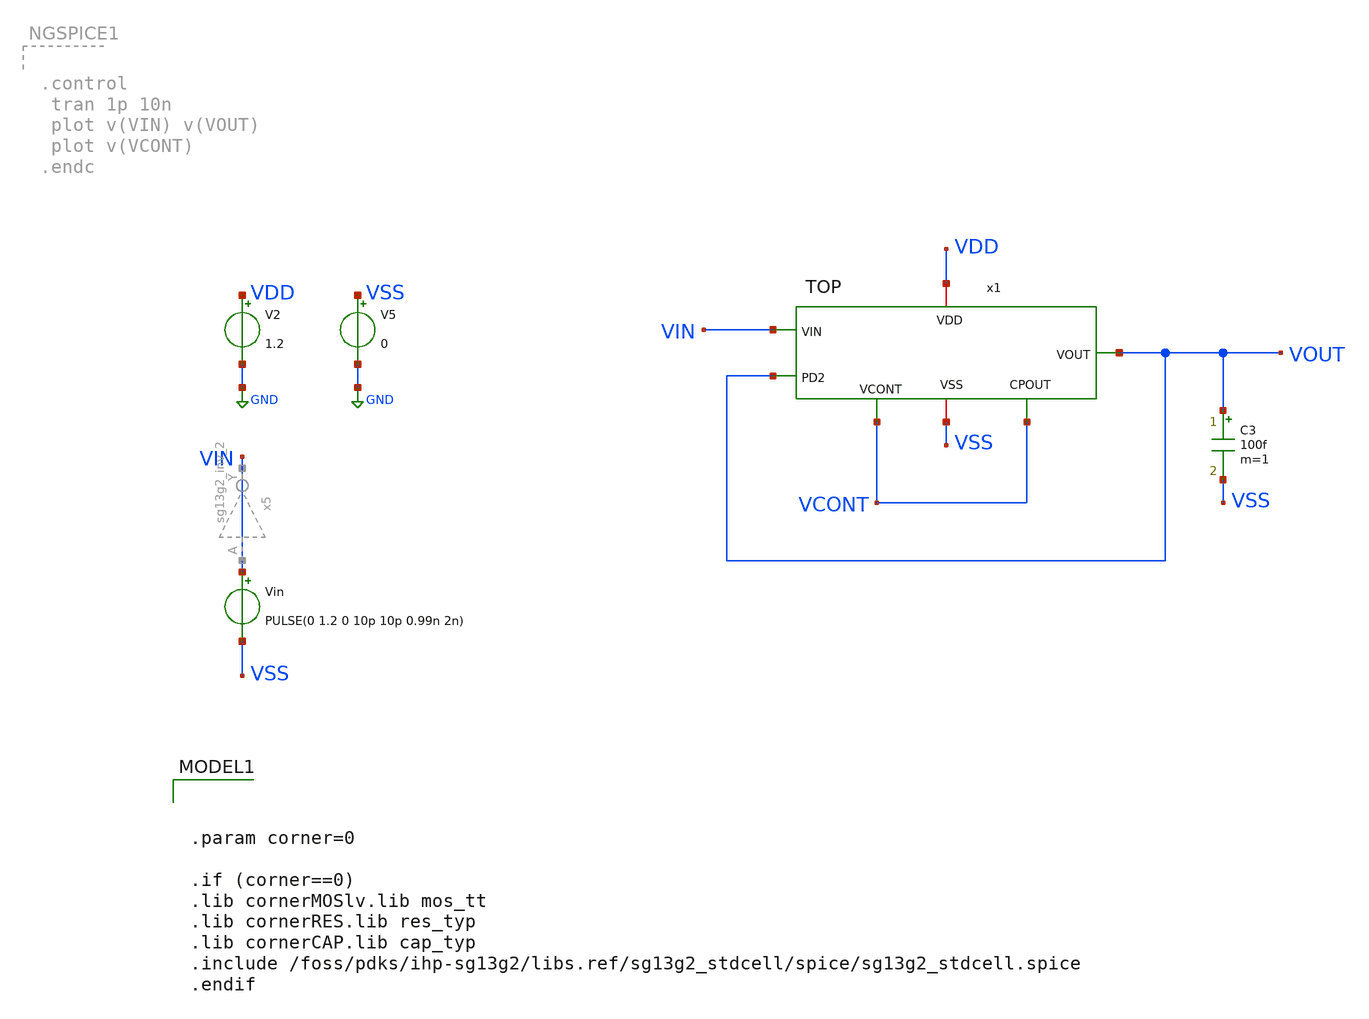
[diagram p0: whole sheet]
** sch_path: xschem/testbenchs/tb_TOP2.sch
**.subckt tb_TOP2
Vin VIN VSS PULSE(0 1.2 0 10p 10p 0.99n 2n)
C3 VOUT VSS 100f m=1
V2 VDD GND 1.2
V5 VSS GND 0
x1 VDD VOUT VIN VCONT VSS VCONT VOUT TOP
**** begin user architecture code


.param corner=0

.if (corner==0)
.lib cornerMOSlv.lib mos_tt
.lib cornerRES.lib res_typ
.lib cornerCAP.lib cap_typ
.include /foss/pdks/ihp-sg13g2/libs.ref/sg13g2_stdcell/spice/sg13g2_stdcell.spice
.endif



.control
 tran 1p 10n
 plot v(VIN) v(VOUT)
 plot v(VCONT)
.endc


**** end user architecture code
**.ends
.GLOBAL GND
.end
